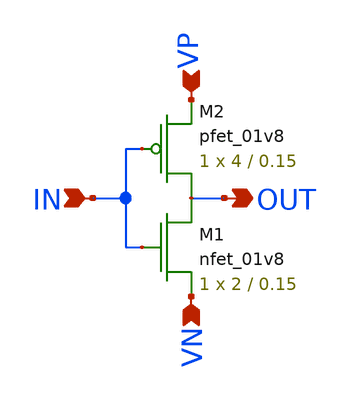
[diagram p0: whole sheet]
** sch_path: Mixed-Signal TRNG/xschem/inv.sch
**.subckt inv IN OUT VP VN
*.ipin IN
*.opin OUT
*.ipin VP
*.ipin VN
XM1 OUT IN VN VN sky130_fd_pr__nfet_01v8 L=0.15 W=2 nf=1 ad='int((nf+1)/2) * W/nf * 0.29' as='int((nf+2)/2) * W/nf * 0.29'
+ pd='2*int((nf+1)/2) * (W/nf + 0.29)' ps='2*int((nf+2)/2) * (W/nf + 0.29)' nrd='0.29 / W' nrs='0.29 / W'
+ sa=0 sb=0 sd=0 mult=1 m=1
XM2 OUT IN VP VP sky130_fd_pr__pfet_01v8 L=0.15 W=4 nf=1 ad='int((nf+1)/2) * W/nf * 0.29' as='int((nf+2)/2) * W/nf * 0.29'
+ pd='2*int((nf+1)/2) * (W/nf + 0.29)' ps='2*int((nf+2)/2) * (W/nf + 0.29)' nrd='0.29 / W' nrs='0.29 / W'
+ sa=0 sb=0 sd=0 mult=1 m=1
**.ends
.end
